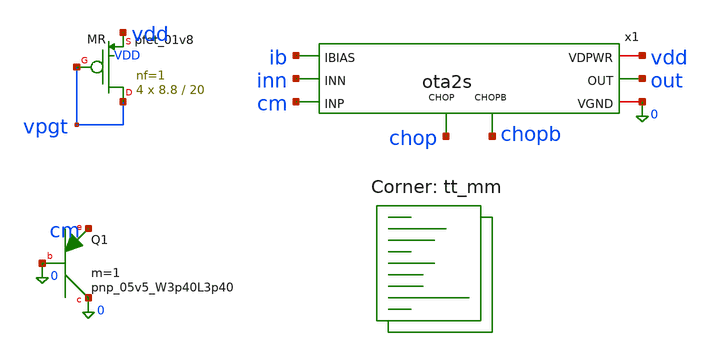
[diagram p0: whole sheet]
** sch_path: xschem/tb_m3_mc.sch
**.subckt tb_m3_mc
x1 cm inn out vdd 0 ib chop chopb ota2s
XMR vpgt vpgt vdd VDD sky130_fd_pr__pfet_01v8 L=20 W=8.8 nf=1 ad='int((1 + 1)/2) * 8.8 / 1 * 0.29' as='int((1 + 2)/2) * 8.8 / 1 * 0.29'
+ pd='2*int((1 + 1)/2) * (8.8 / 1 + 0.29)' ps='2*int((1 + 2)/2) * (8.8 / 1 + 0.29)' nrd='0.29 / 8.8 ' nrs='0.29 / 8.8 '
+ sa=0 sb=0 sd=0 mult=4 m=4
XQ1 0 0 cm sky130_fd_pr__pnp_05v5_W3p40L3p40 m=1
**** begin user architecture code
.lib $::SKYWATER_MODELS/sky130.lib.spice tt_mm

.param vdd=1.8 rs=1
.temp 25
Vdd vdd 0 {vdd}
* door 1: input CM = a real diode PNP carrying I_PTAT(T)
* rs = R1 corner (1 nominal, 1.17 ll, 0.88 hh); the denominator is R1's own tempco
Bcm vdd cm I = 2.79e-6*rs*(temper+273.15)/298.15/(1+4.89e-4*(temper-27)+1.2e-6*(temper-27)**2)
* door 2: PTAT bias, I_PTAT/2, sunk from IBIAS
Bib ib 0 I = 1.40e-6*rs*(temper+273.15)/298.15/(1+4.89e-4*(temper-27)+1.2e-6*(temper-27)**2)
* door 4: replica P1 carries I_PTAT -> its gate is the vpg target
Brp vpgt 0 I = 2.79e-6*rs*(temper+273.15)/298.15/(1+4.89e-4*(temper-27)+1.2e-6*(temper-27)**2)
* chop state A (swap the two values for state B)
Vchop chop 0 0
Vchopb chopb 0 {vdd}
* servo: plays the bandgap loop, moves INN until out = vpgt
Bsv inn cm V = 0.5*tanh(2000*(v(out)-v(vpgt)))
.control
setseed 42
let nmax = 200
let v25 = vector(nmax)
let vm20 = vector(nmax)
let v100 = vector(nmax)
let v171 = vector(nmax)
let v189 = vector(nmax)
let n = 0
while n < nmax
  reset
  option reltol=1e-5 vntol=1e-9
  option temp=25
  op
  let v25[n] = v(cm)-v(inn)
  option temp=-20
  op
  let vm20[n] = v(cm)-v(inn)
  option temp=100
  op
  let v100[n] = v(cm)-v(inn)
  option temp=25
  alter vdd dc=1.71
  alter vchopb dc=1.71
  op
  let v171[n] = v(cm)-v(inn)
  alter vdd dc=1.89
  alter vchopb dc=1.89
  op
  let v189[n] = v(cm)-v(inn)
  let n = n + 1
end
setplot const
let m25 = mean(v25)*1e6
let s25 = sqrt(mean((v25-mean(v25))^2)*nmax/(nmax-1))*1e6
let up95 = 1.09*s25
let dc = vm20-v25
let dh = v100-v25
let sdc = sqrt(mean((dc-mean(dc))^2)*nmax/(nmax-1))*1e6
let sdh = sqrt(mean((dh-mean(dh))^2)*nmax/(nmax-1))*1e6
let ps = (v189-v171)/0.18*1e6
let psm = mean(ps)
let psw = vecmax(abs(ps))
echo MCRESULT corner=tt_mm seed=42 N=$&nmax mean_uV=$&m25 sigma_uV=$&s25 up95_uV=$&up95 drift_m20_sigma_uV=$&sdc drift_100_sigma_uV=$&sdh psrr_mean_uVperV=$&psm psrr_worst_uVperV=$&psw
let sample = vector(nmax)
setscale sample
wrdata mc_tt_mm_42.csv v25 vm20 v100 v171 v189
.endc

**** end user architecture code
**.ends

* expanding   symbol:  ota2s.sym # of pins=8
** sym_path: xschem/ota2s.sym
** sch_path: xschem/ota2s.sch
.subckt ota2s INP INN OUT VDPWR VGND IBIAS CHOP CHOPB
*.ipin INN
*.ipin INP
*.ipin IBIAS
*.opin OUT
*.iopin VDPWR
*.iopin VGND
*.ipin CHOPB
*.ipin CHOP
XMREF IBIAS IBIAS VDPWR VDPWR sky130_fd_pr__pfet_01v8 L=4 W=20 nf=1 ad='int((1 + 1)/2) * 20 / 1 * 0.29' as='int((1
+ + 2)/2) * 20 / 1 * 0.29' pd='2*int((1 + 1)/2) * (20 / 1 + 0.29)' ps='2*int((1 + 2)/2) * (20 / 1 + 0.29)' nrd='0.29
+ / 20 ' nrs='0.29 / 20 ' sa=0 sb=0 sd=0 mult=1 m=1
XMTAIL tail IBIAS VDPWR VDPWR sky130_fd_pr__pfet_01v8 L=4 W=20 nf=1 ad='int((1 + 1)/2) * 20 / 1 * 0.29' as='int((1
+ + 2)/2) * 20 / 1 * 0.29' pd='2*int((1 + 1)/2) * (20 / 1 + 0.29)' ps='2*int((1 + 2)/2) * (20 / 1 + 0.29)' nrd='0.29
+ / 20 ' nrs='0.29 / 20 ' sa=0 sb=0 sd=0 mult=2 m=2
XMP1 d1 INN tail VDPWR sky130_fd_pr__pfet_01v8_lvt L=6 W=25 nf=1 ad='int((1 + 1)/2) * 25 / 1 * 0.29' as='int((1
+ + 2)/2) * 25 / 1 * 0.29' pd='2*int((1 + 1)/2) * (25 / 1 + 0.29)' ps='2*int((1 + 2)/2) * (25 / 1 + 0.29)' nrd='0.29
+ / 25 ' nrs='0.29 / 25 ' sa=0 sb=0 sd=0 mult=24 m=24
XMP2 x1 INP tail VDPWR sky130_fd_pr__pfet_01v8_lvt L=6 W=25 nf=1 ad='int((1 + 1)/2) * 25 / 1 * 0.29' as='int((1
+ + 2)/2) * 25 / 1 * 0.29' pd='2*int((1 + 1)/2) * (25 / 1 + 0.29)' ps='2*int((1 + 2)/2) * (25 / 1 + 0.29)' nrd='0.29
+ / 25 ' nrs='0.29 / 25 ' sa=0 sb=0 sd=0 mult=24 m=24
XMN1 d1 g12 VGND VGND sky130_fd_pr__nfet_01v8 L=20 W=6 nf=1 ad='int((1 + 1)/2) * 6 / 1 * 0.29' as='int((1
+ + 2)/2) * 6 / 1 * 0.29' pd='2*int((1 + 1)/2) * (6 / 1 + 0.29)' ps='2*int((1 + 2)/2) * (6 / 1 + 0.29)' nrd='0.29
+ / 6 ' nrs='0.29 / 6 ' sa=0 sb=0 sd=0 mult=2 m=2
XMN2 x1 g12 VGND VGND sky130_fd_pr__nfet_01v8 L=20 W=6 nf=1 ad='int((1 + 1)/2) * 6 / 1 * 0.29' as='int((1
+ + 2)/2) * 6 / 1 * 0.29' pd='2*int((1 + 1)/2) * (6 / 1 + 0.29)' ps='2*int((1 + 2)/2) * (6 / 1 + 0.29)' nrd='0.29
+ / 6 ' nrs='0.29 / 6 ' sa=0 sb=0 sd=0 mult=2 m=2
XMP3 OUT IBIAS VDPWR VDPWR sky130_fd_pr__pfet_01v8 L=4 W=20 nf=1 ad='int((1 + 1)/2) * 20 / 1 * 0.29' as='int((1
+ + 2)/2) * 20 / 1 * 0.29' pd='2*int((1 + 1)/2) * (20 / 1 + 0.29)' ps='2*int((1 + 2)/2) * (20 / 1 + 0.29)' nrd='0.29
+ / 20 ' nrs='0.29 / 20 ' sa=0 sb=0 sd=0 mult=6 m=6
XMN3 OUT g3 VGND VGND sky130_fd_pr__nfet_01v8 L=1 W=7 nf=1 ad='int((1 + 1)/2) * 7 / 1 * 0.29' as='int((1
+ + 2)/2) * 7 / 1 * 0.29' pd='2*int((1 + 1)/2) * (7 / 1 + 0.29)' ps='2*int((1 + 2)/2) * (7 / 1 + 0.29)' nrd='0.29
+ / 7 ' nrs='0.29 / 7 ' sa=0 sb=0 sd=0 mult=1 m=1
XRZ1 net1 g3 VGND sky130_fd_pr__res_high_po_1p41 L=20 mult=1 m=1
XRZ2 net2 net1 VGND sky130_fd_pr__res_high_po_1p41 L=20 mult=1 m=1
XRZ3 net3 net2 VGND sky130_fd_pr__res_high_po_1p41 L=20 mult=1 m=1
XRZ4 net4 net3 VGND sky130_fd_pr__res_high_po_1p41 L=20 mult=1 m=1
XRZ5 net5 net4 VGND sky130_fd_pr__res_high_po_1p41 L=20 mult=1 m=1
XRZ6 cz net5 VGND sky130_fd_pr__res_high_po_1p41 L=20 mult=1 m=1
XCC cz OUT sky130_fd_pr__cap_mim_m3_1 W=25 L=25 MF=8 m=8
XDP tail VDPWR tail VDPWR sky130_fd_pr__pfet_01v8_lvt L=6 W=25 nf=1 ad='int((1 + 1)/2) * 25 / 1 * 0.29' as='int((1
+ + 2)/2) * 25 / 1 * 0.29' pd='2*int((1 + 1)/2) * (25 / 1 + 0.29)' ps='2*int((1 + 2)/2) * (25 / 1 + 0.29)' nrd='0.29
+ / 25 ' nrs='0.29 / 25 ' sa=0 sb=0 sd=0 mult=8 m=8
XDNA d1 VGND VGND VGND sky130_fd_pr__nfet_01v8 L=20 W=6 nf=1 ad='int((1 + 1)/2) * 6 / 1 * 0.29' as='int((1
+ + 2)/2) * 6 / 1 * 0.29' pd='2*int((1 + 1)/2) * (6 / 1 + 0.29)' ps='2*int((1 + 2)/2) * (6 / 1 + 0.29)' nrd='0.29
+ / 6 ' nrs='0.29 / 6 ' sa=0 sb=0 sd=0 mult=2 m=2
XDNB x1 VGND VGND VGND sky130_fd_pr__nfet_01v8 L=20 W=6 nf=1 ad='int((1 + 1)/2) * 6 / 1 * 0.29' as='int((1
+ + 2)/2) * 6 / 1 * 0.29' pd='2*int((1 + 1)/2) * (6 / 1 + 0.29)' ps='2*int((1 + 2)/2) * (6 / 1 + 0.29)' nrd='0.29
+ / 6 ' nrs='0.29 / 6 ' sa=0 sb=0 sd=0 mult=2 m=2
XDB VDPWR VDPWR VDPWR VDPWR sky130_fd_pr__pfet_01v8 L=4 W=20 nf=1 ad='int((1 + 1)/2) * 20 / 1 * 0.29' as='int((1
+ + 2)/2) * 20 / 1 * 0.29' pd='2*int((1 + 1)/2) * (20 / 1 + 0.29)' ps='2*int((1 + 2)/2) * (20 / 1 + 0.29)' nrd='0.29
+ / 20 ' nrs='0.29 / 20 ' sa=0 sb=0 sd=0 mult=2 m=2
XRD1 VGND VGND VGND sky130_fd_pr__res_high_po_1p41 L=20 mult=1 m=1
XRD2 VGND VGND VGND sky130_fd_pr__res_high_po_1p41 L=20 mult=1 m=1
XSD1 d1 CHOPB g12 VGND sky130_fd_pr__nfet_01v8 L=0.5 W=6 nf=1 ad='int((1 + 1)/2) * 6 / 1 * 0.29' as='int((1
+ + 2)/2) * 6 / 1 * 0.29' pd='2*int((1 + 1)/2) * (6 / 1 + 0.29)' ps='2*int((1 + 2)/2) * (6 / 1 + 0.29)' nrd='0.29
+ / 6 ' nrs='0.29 / 6 ' sa=0 sb=0 sd=0 mult=1 m=1
XSD2 x1 CHOP g12 VGND sky130_fd_pr__nfet_01v8 L=0.5 W=6 nf=1 ad='int((1 + 1)/2) * 6 / 1 * 0.29' as='int((1
+ + 2)/2) * 6 / 1 * 0.29' pd='2*int((1 + 1)/2) * (6 / 1 + 0.29)' ps='2*int((1 + 2)/2) * (6 / 1 + 0.29)' nrd='0.29
+ / 6 ' nrs='0.29 / 6 ' sa=0 sb=0 sd=0 mult=1 m=1
XSG2 g3 CHOP d1 VGND sky130_fd_pr__nfet_01v8 L=0.5 W=6 nf=1 ad='int((1 + 1)/2) * 6 / 1 * 0.29' as='int((1
+ + 2)/2) * 6 / 1 * 0.29' pd='2*int((1 + 1)/2) * (6 / 1 + 0.29)' ps='2*int((1 + 2)/2) * (6 / 1 + 0.29)' nrd='0.29
+ / 6 ' nrs='0.29 / 6 ' sa=0 sb=0 sd=0 mult=1 m=1
XSG1 x1 CHOPB g3 VGND sky130_fd_pr__nfet_01v8 L=0.5 W=6 nf=1 ad='int((1 + 1)/2) * 6 / 1 * 0.29' as='int((1
+ + 2)/2) * 6 / 1 * 0.29' pd='2*int((1 + 1)/2) * (6 / 1 + 0.29)' ps='2*int((1 + 2)/2) * (6 / 1 + 0.29)' nrd='0.29
+ / 6 ' nrs='0.29 / 6 ' sa=0 sb=0 sd=0 mult=1 m=1
.ends

.end
